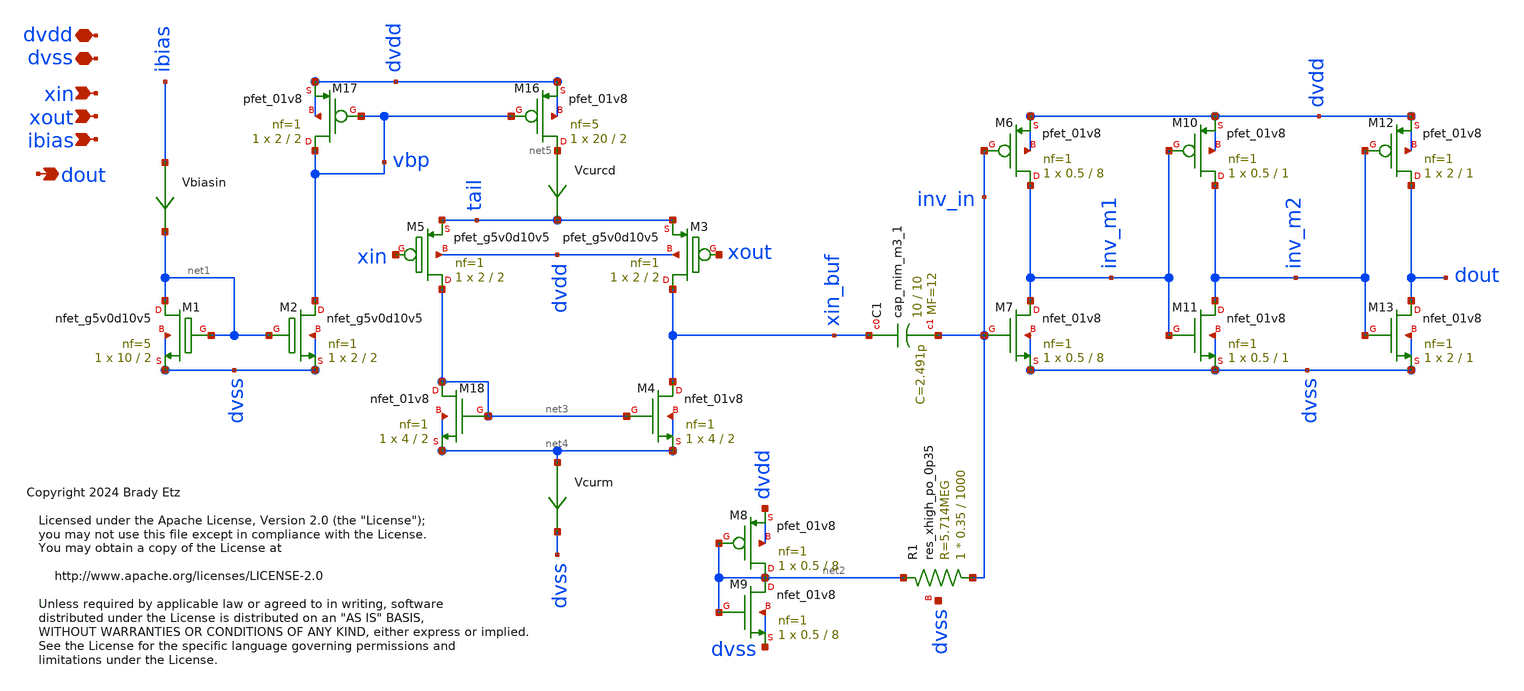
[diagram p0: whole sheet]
** sch_path: xschem/dout_amp_d.sch
* Copyright 2024 Brady Etz
* Licensed under the Apache License, Version 2.0 (the "License");
**.subckt dout_amp_d xin dvdd dvss dout ibias xout
*.ipin xin
*.iopin dvdd
*.iopin dvss
*.opin dout
*.ipin ibias
*.ipin xout
XM1 net1 net1 dvss dvss sky130_fd_pr__nfet_g5v0d10v5 L=2 W=10 nf=5 ad='int((nf+1)/2) * W/nf * 0.29' as='int((nf+2)/2) * W/nf * 0.29'
+ pd='2*int((nf+1)/2) * (W/nf + 0.29)' ps='2*int((nf+2)/2) * (W/nf + 0.29)' nrd='0.29 / W' nrs='0.29 / W'
+ sa=0 sb=0 sd=0 mult=1 m=1
XM2 vbp net1 dvss dvss sky130_fd_pr__nfet_g5v0d10v5 L=2 W=2 nf=1 ad='int((nf+1)/2) * W/nf * 0.29' as='int((nf+2)/2) * W/nf * 0.29'
+ pd='2*int((nf+1)/2) * (W/nf + 0.29)' ps='2*int((nf+2)/2) * (W/nf + 0.29)' nrd='0.29 / W' nrs='0.29 / W'
+ sa=0 sb=0 sd=0 mult=1 m=1
XM5 net3 xin tail dvdd sky130_fd_pr__pfet_g5v0d10v5 L=2 W=2 nf=1 ad='int((nf+1)/2) * W/nf * 0.29' as='int((nf+2)/2) * W/nf * 0.29'
+ pd='2*int((nf+1)/2) * (W/nf + 0.29)' ps='2*int((nf+2)/2) * (W/nf + 0.29)' nrd='0.29 / W' nrs='0.29 / W'
+ sa=0 sb=0 sd=0 mult=1 m=1
XC1 xin_buf inv_in sky130_fd_pr__cap_mim_m3_1 W=10 L=10 MF=12 m=12
XM6 inv_m1 inv_in dvdd dvdd sky130_fd_pr__pfet_01v8 L=8 W=0.5 nf=1 ad='int((nf+1)/2) * W/nf * 0.29' as='int((nf+2)/2) * W/nf * 0.29'
+ pd='2*int((nf+1)/2) * (W/nf + 0.29)' ps='2*int((nf+2)/2) * (W/nf + 0.29)' nrd='0.29 / W' nrs='0.29 / W'
+ sa=0 sb=0 sd=0 mult=1 m=1
XM7 inv_m1 inv_in dvss dvss sky130_fd_pr__nfet_01v8 L=8 W=0.5 nf=1 ad='int((nf+1)/2) * W/nf * 0.29' as='int((nf+2)/2) * W/nf * 0.29'
+ pd='2*int((nf+1)/2) * (W/nf + 0.29)' ps='2*int((nf+2)/2) * (W/nf + 0.29)' nrd='0.29 / W' nrs='0.29 / W'
+ sa=0 sb=0 sd=0 mult=1 m=1
XM8 net2 net2 dvdd dvdd sky130_fd_pr__pfet_01v8 L=8 W=0.5 nf=1 ad='int((nf+1)/2) * W/nf * 0.29' as='int((nf+2)/2) * W/nf * 0.29'
+ pd='2*int((nf+1)/2) * (W/nf + 0.29)' ps='2*int((nf+2)/2) * (W/nf + 0.29)' nrd='0.29 / W' nrs='0.29 / W'
+ sa=0 sb=0 sd=0 mult=1 m=1
XM9 net2 net2 dvss dvss sky130_fd_pr__nfet_01v8 L=8 W=0.5 nf=1 ad='int((nf+1)/2) * W/nf * 0.29' as='int((nf+2)/2) * W/nf * 0.29'
+ pd='2*int((nf+1)/2) * (W/nf + 0.29)' ps='2*int((nf+2)/2) * (W/nf + 0.29)' nrd='0.29 / W' nrs='0.29 / W'
+ sa=0 sb=0 sd=0 mult=1 m=1
XR1 inv_in net2 dvss sky130_fd_pr__res_xhigh_po_0p35 L=1000 mult=1 m=1
XM10 inv_m2 inv_m1 dvdd dvdd sky130_fd_pr__pfet_01v8 L=1 W=0.5 nf=1 ad='int((nf+1)/2) * W/nf * 0.29'
+ as='int((nf+2)/2) * W/nf * 0.29' pd='2*int((nf+1)/2) * (W/nf + 0.29)' ps='2*int((nf+2)/2) * (W/nf + 0.29)'
+ nrd='0.29 / W' nrs='0.29 / W' sa=0 sb=0 sd=0 mult=1 m=1
XM11 inv_m2 inv_m1 dvss dvss sky130_fd_pr__nfet_01v8 L=1 W=0.5 nf=1 ad='int((nf+1)/2) * W/nf * 0.29'
+ as='int((nf+2)/2) * W/nf * 0.29' pd='2*int((nf+1)/2) * (W/nf + 0.29)' ps='2*int((nf+2)/2) * (W/nf + 0.29)'
+ nrd='0.29 / W' nrs='0.29 / W' sa=0 sb=0 sd=0 mult=1 m=1
XM12 dout inv_m2 dvdd dvdd sky130_fd_pr__pfet_01v8 L=1 W=2 nf=1 ad='int((nf+1)/2) * W/nf * 0.29' as='int((nf+2)/2) * W/nf * 0.29'
+ pd='2*int((nf+1)/2) * (W/nf + 0.29)' ps='2*int((nf+2)/2) * (W/nf + 0.29)' nrd='0.29 / W' nrs='0.29 / W'
+ sa=0 sb=0 sd=0 mult=1 m=1
XM13 dout inv_m2 dvss dvss sky130_fd_pr__nfet_01v8 L=1 W=2 nf=1 ad='int((nf+1)/2) * W/nf * 0.29' as='int((nf+2)/2) * W/nf * 0.29'
+ pd='2*int((nf+1)/2) * (W/nf + 0.29)' ps='2*int((nf+2)/2) * (W/nf + 0.29)' nrd='0.29 / W' nrs='0.29 / W'
+ sa=0 sb=0 sd=0 mult=1 m=1
Vcurcd net5 tail 0
.save i(vcurcd)
Vbiasin ibias net1 0
.save i(vbiasin)
XM16 net5 vbp dvdd dvdd sky130_fd_pr__pfet_01v8 L=2 W=20 nf=5 ad='int((nf+1)/2) * W/nf * 0.29' as='int((nf+2)/2) * W/nf * 0.29'
+ pd='2*int((nf+1)/2) * (W/nf + 0.29)' ps='2*int((nf+2)/2) * (W/nf + 0.29)' nrd='0.29 / W' nrs='0.29 / W'
+ sa=0 sb=0 sd=0 mult=1 m=1
XM17 vbp vbp dvdd dvdd sky130_fd_pr__pfet_01v8 L=2 W=2 nf=1 ad='int((nf+1)/2) * W/nf * 0.29' as='int((nf+2)/2) * W/nf * 0.29'
+ pd='2*int((nf+1)/2) * (W/nf + 0.29)' ps='2*int((nf+2)/2) * (W/nf + 0.29)' nrd='0.29 / W' nrs='0.29 / W'
+ sa=0 sb=0 sd=0 mult=1 m=1
XM3 xin_buf xout tail dvdd sky130_fd_pr__pfet_g5v0d10v5 L=2 W=2 nf=1 ad='int((nf+1)/2) * W/nf * 0.29'
+ as='int((nf+2)/2) * W/nf * 0.29' pd='2*int((nf+1)/2) * (W/nf + 0.29)' ps='2*int((nf+2)/2) * (W/nf + 0.29)'
+ nrd='0.29 / W' nrs='0.29 / W' sa=0 sb=0 sd=0 mult=1 m=1
XM4 xin_buf net3 net4 net4 sky130_fd_pr__nfet_01v8 L=2 W=4 nf=1 ad='int((nf+1)/2) * W/nf * 0.29' as='int((nf+2)/2) * W/nf * 0.29'
+ pd='2*int((nf+1)/2) * (W/nf + 0.29)' ps='2*int((nf+2)/2) * (W/nf + 0.29)' nrd='0.29 / W' nrs='0.29 / W'
+ sa=0 sb=0 sd=0 mult=1 m=1
XM18 net3 net3 net4 net4 sky130_fd_pr__nfet_01v8 L=2 W=4 nf=1 ad='int((nf+1)/2) * W/nf * 0.29' as='int((nf+2)/2) * W/nf * 0.29'
+ pd='2*int((nf+1)/2) * (W/nf + 0.29)' ps='2*int((nf+2)/2) * (W/nf + 0.29)' nrd='0.29 / W' nrs='0.29 / W'
+ sa=0 sb=0 sd=0 mult=1 m=1
Vcurm net4 dvss 0
.save i(vcurm)
**.ends
.end
